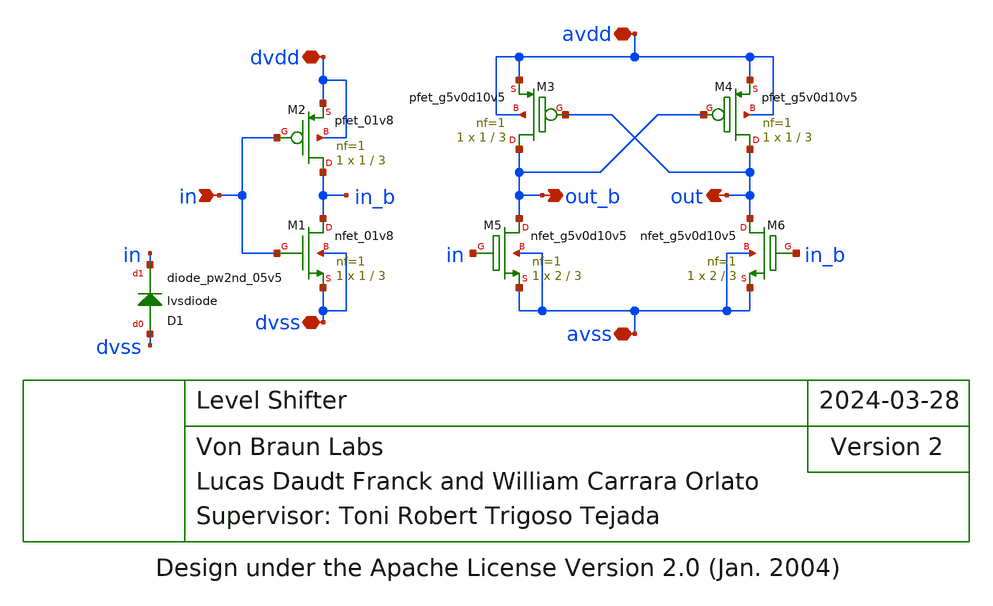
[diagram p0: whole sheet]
** sch_path: blocks/Level-Shifter/xschen/level_shifter.sch
* Design under the Apache License Version 2.0 (Jan. 2004)
**.subckt level_shifter avdd out_b out avss dvdd in dvss
*.iopin avdd
*.opin out_b
*.opin out
*.iopin avss
*.iopin dvdd
*.ipin in
*.iopin dvss
XM1 in_b in dvss dvss sky130_fd_pr__nfet_01v8 L=3 W=1 nf=1 ad='int((nf+1)/2) * W/nf * 0.29' as='int((nf+2)/2) * W/nf * 0.29'
+ pd='2*int((nf+1)/2) * (W/nf + 0.29)' ps='2*int((nf+2)/2) * (W/nf + 0.29)' nrd='0.29 / W' nrs='0.29 / W'
+ sa=0 sb=0 sd=0 mult=1 m=1
XM2 in_b in dvdd dvdd sky130_fd_pr__pfet_01v8 L=3 W=1 nf=1 ad='int((nf+1)/2) * W/nf * 0.29' as='int((nf+2)/2) * W/nf * 0.29'
+ pd='2*int((nf+1)/2) * (W/nf + 0.29)' ps='2*int((nf+2)/2) * (W/nf + 0.29)' nrd='0.29 / W' nrs='0.29 / W'
+ sa=0 sb=0 sd=0 mult=1 m=1
XM3 out_b out avdd avdd sky130_fd_pr__pfet_g5v0d10v5 L=3 W=1 nf=1 ad='int((nf+1)/2) * W/nf * 0.29' as='int((nf+2)/2) * W/nf * 0.29'
+ pd='2*int((nf+1)/2) * (W/nf + 0.29)' ps='2*int((nf+2)/2) * (W/nf + 0.29)' nrd='0.29 / W' nrs='0.29 / W'
+ sa=0 sb=0 sd=0 mult=1 m=1
XM4 out out_b avdd avdd sky130_fd_pr__pfet_g5v0d10v5 L=3 W=1 nf=1 ad='int((nf+1)/2) * W/nf * 0.29' as='int((nf+2)/2) * W/nf * 0.29'
+ pd='2*int((nf+1)/2) * (W/nf + 0.29)' ps='2*int((nf+2)/2) * (W/nf + 0.29)' nrd='0.29 / W' nrs='0.29 / W'
+ sa=0 sb=0 sd=0 mult=1 m=1
XM6 out in_b avss avss sky130_fd_pr__nfet_g5v0d10v5 L=3 W=2 nf=1 ad='int((nf+1)/2) * W/nf * 0.29' as='int((nf+2)/2) * W/nf * 0.29'
+ pd='2*int((nf+1)/2) * (W/nf + 0.29)' ps='2*int((nf+2)/2) * (W/nf + 0.29)' nrd='0.29 / W' nrs='0.29 / W'
+ sa=0 sb=0 sd=0 mult=1 m=1
XM5 out_b in avss avss sky130_fd_pr__nfet_g5v0d10v5 L=3 W=2 nf=1 ad='int((nf+1)/2) * W/nf * 0.29' as='int((nf+2)/2) * W/nf * 0.29'
+ pd='2*int((nf+1)/2) * (W/nf + 0.29)' ps='2*int((nf+2)/2) * (W/nf + 0.29)' nrd='0.29 / W' nrs='0.29 / W'
+ sa=0 sb=0 sd=0 mult=1 m=1
D1 dvss in sky130_fd_pr__diode_pw2nd_05v5 area=0.315e12
**.ends
.end
